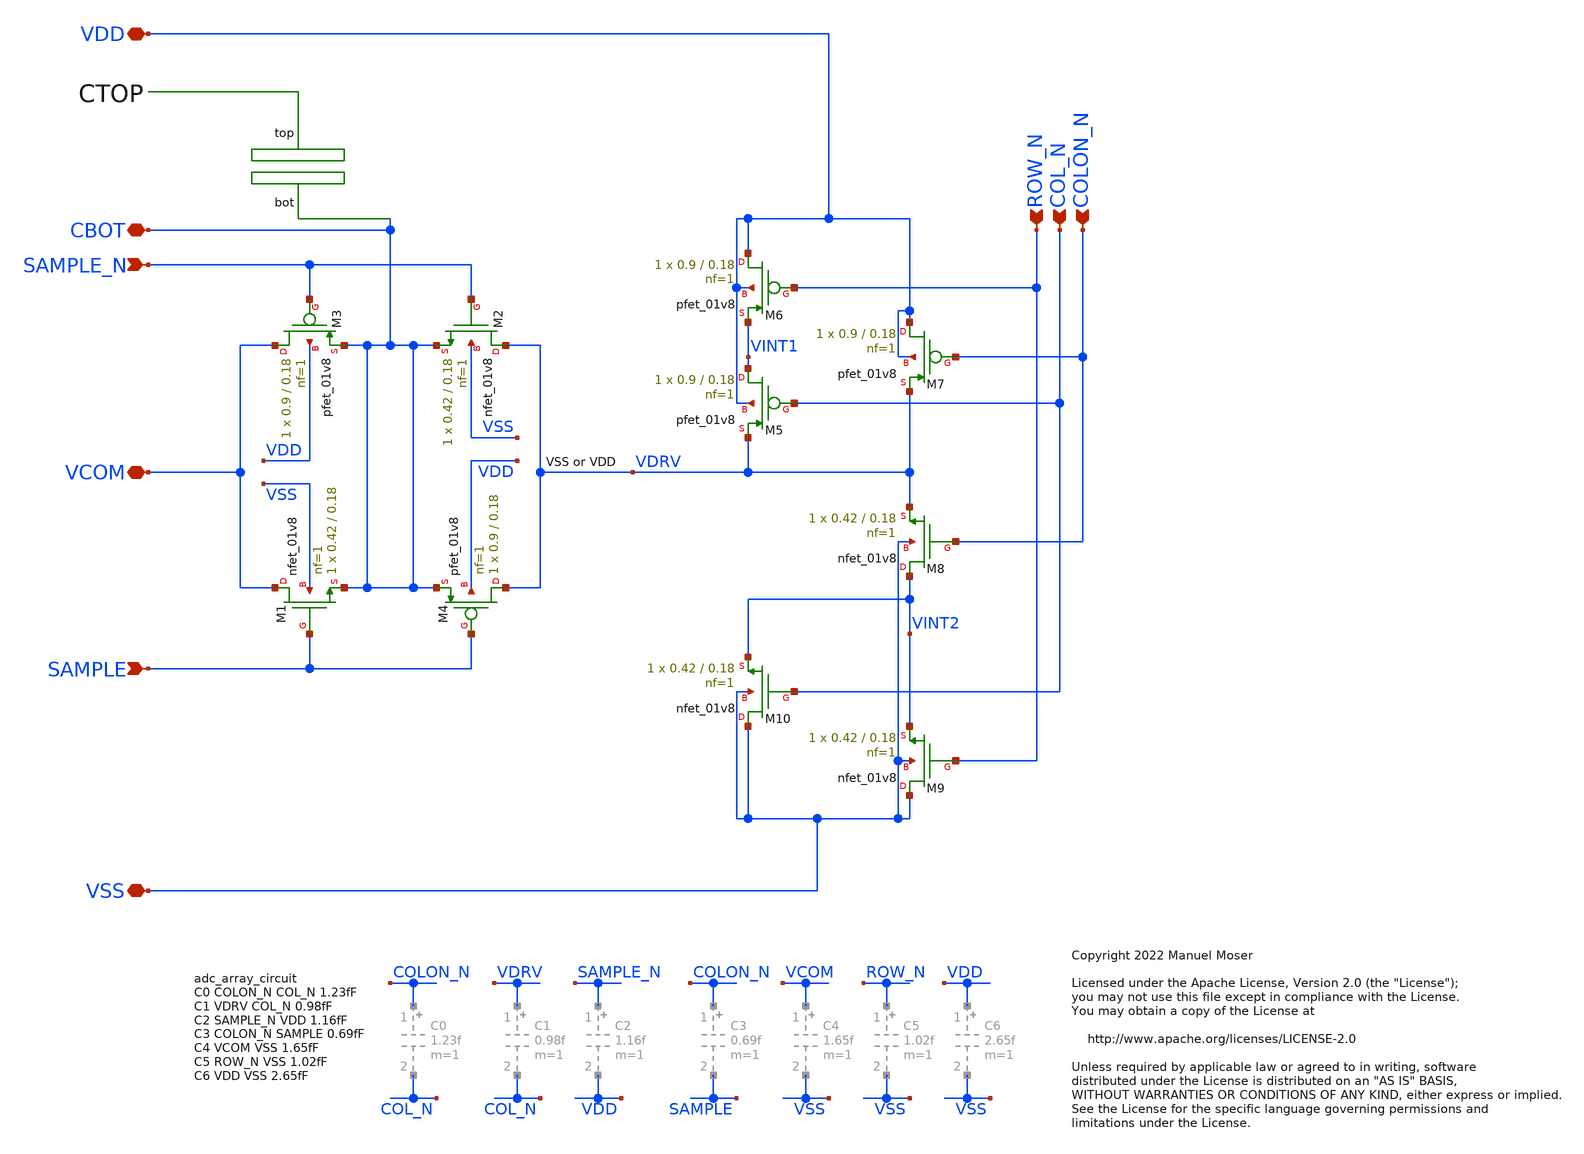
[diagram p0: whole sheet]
** sch_path: xschem/adc_array_circuit_180n/adc_array_circuit_180n.sch
* Copyright 2022 Manuel Moser
* Licensed under the Apache License, Version 2.0 (the "License");
**.subckt adc_array_circuit_180n SAMPLE_N SAMPLE VCOM ROW_N COL_N COLON_N VDD VSS CBOT
*.ipin SAMPLE_N
*.ipin SAMPLE
*.iopin VCOM
*.ipin ROW_N
*.ipin COL_N
*.ipin COLON_N
*.iopin VDD
*.iopin VSS
*.iopin CBOT
XM1 VCOM SAMPLE CBOT VSS sky130_fd_pr__nfet_01v8 L=0.18 W=0.42 nf=1 ad='int((nf+1)/2) * W/nf * 0.29'
+ as='int((nf+2)/2) * W/nf * 0.29' pd='2*int((nf+1)/2) * (W/nf + 0.29)' ps='2*int((nf+2)/2) * (W/nf + 0.29)'
+ nrd='0.29 / W' nrs='0.29 / W' sa=0 sb=0 sd=0 mult=1 m=1
XM3 VCOM SAMPLE_N CBOT VDD sky130_fd_pr__pfet_01v8 L=0.18 W=0.9 nf=1 ad='int((nf+1)/2) * W/nf * 0.29'
+ as='int((nf+2)/2) * W/nf * 0.29' pd='2*int((nf+1)/2) * (W/nf + 0.29)' ps='2*int((nf+2)/2) * (W/nf + 0.29)'
+ nrd='0.29 / W' nrs='0.29 / W' sa=0 sb=0 sd=0 mult=1 m=1
XM2 VDRV SAMPLE_N CBOT VSS sky130_fd_pr__nfet_01v8 L=0.18 W=0.42 nf=1 ad='int((nf+1)/2) * W/nf * 0.29'
+ as='int((nf+2)/2) * W/nf * 0.29' pd='2*int((nf+1)/2) * (W/nf + 0.29)' ps='2*int((nf+2)/2) * (W/nf + 0.29)'
+ nrd='0.29 / W' nrs='0.29 / W' sa=0 sb=0 sd=0 mult=1 m=1
XM4 VDRV SAMPLE CBOT VDD sky130_fd_pr__pfet_01v8 L=0.18 W=0.9 nf=1 ad='int((nf+1)/2) * W/nf * 0.29' as='int((nf+2)/2) * W/nf * 0.29'
+ pd='2*int((nf+1)/2) * (W/nf + 0.29)' ps='2*int((nf+2)/2) * (W/nf + 0.29)' nrd='0.29 / W' nrs='0.29 / W'
+ sa=0 sb=0 sd=0 mult=1 m=1
XM5 VINT1 COL_N VDRV VDD sky130_fd_pr__pfet_01v8 L=0.18 W=0.9 nf=1 ad='int((nf+1)/2) * W/nf * 0.29' as='int((nf+2)/2) * W/nf * 0.29'
+ pd='2*int((nf+1)/2) * (W/nf + 0.29)' ps='2*int((nf+2)/2) * (W/nf + 0.29)' nrd='0.29 / W' nrs='0.29 / W'
+ sa=0 sb=0 sd=0 mult=1 m=1
XM6 VDD ROW_N VINT1 VDD sky130_fd_pr__pfet_01v8 L=0.18 W=0.9 nf=1 ad='int((nf+1)/2) * W/nf * 0.29' as='int((nf+2)/2) * W/nf * 0.29'
+ pd='2*int((nf+1)/2) * (W/nf + 0.29)' ps='2*int((nf+2)/2) * (W/nf + 0.29)' nrd='0.29 / W' nrs='0.29 / W'
+ sa=0 sb=0 sd=0 mult=1 m=1
XM7 VDD COLON_N VDRV VDD sky130_fd_pr__pfet_01v8 L=0.18 W=0.9 nf=1 ad='int((nf+1)/2) * W/nf * 0.29' as='int((nf+2)/2) * W/nf * 0.29'
+ pd='2*int((nf+1)/2) * (W/nf + 0.29)' ps='2*int((nf+2)/2) * (W/nf + 0.29)' nrd='0.29 / W' nrs='0.29 / W'
+ sa=0 sb=0 sd=0 mult=1 m=1
XM8 VINT2 COLON_N VDRV VSS sky130_fd_pr__nfet_01v8 L=0.18 W=0.42 nf=1 ad='int((nf+1)/2) * W/nf * 0.29'
+ as='int((nf+2)/2) * W/nf * 0.29' pd='2*int((nf+1)/2) * (W/nf + 0.29)' ps='2*int((nf+2)/2) * (W/nf + 0.29)'
+ nrd='0.29 / W' nrs='0.29 / W' sa=0 sb=0 sd=0 mult=1 m=1
XM9 VSS ROW_N VINT2 VSS sky130_fd_pr__nfet_01v8 L=0.18 W=0.42 nf=1 ad='int((nf+1)/2) * W/nf * 0.29' as='int((nf+2)/2) * W/nf * 0.29'
+ pd='2*int((nf+1)/2) * (W/nf + 0.29)' ps='2*int((nf+2)/2) * (W/nf + 0.29)' nrd='0.29 / W' nrs='0.29 / W'
+ sa=0 sb=0 sd=0 mult=1 m=1
XM10 VSS COL_N VINT2 VSS sky130_fd_pr__nfet_01v8 L=0.18 W=0.42 nf=1 ad='int((nf+1)/2) * W/nf * 0.29'
+ as='int((nf+2)/2) * W/nf * 0.29' pd='2*int((nf+1)/2) * (W/nf + 0.29)' ps='2*int((nf+2)/2) * (W/nf + 0.29)'
+ nrd='0.29 / W' nrs='0.29 / W' sa=0 sb=0 sd=0 mult=1 m=1
**.ends
.end
